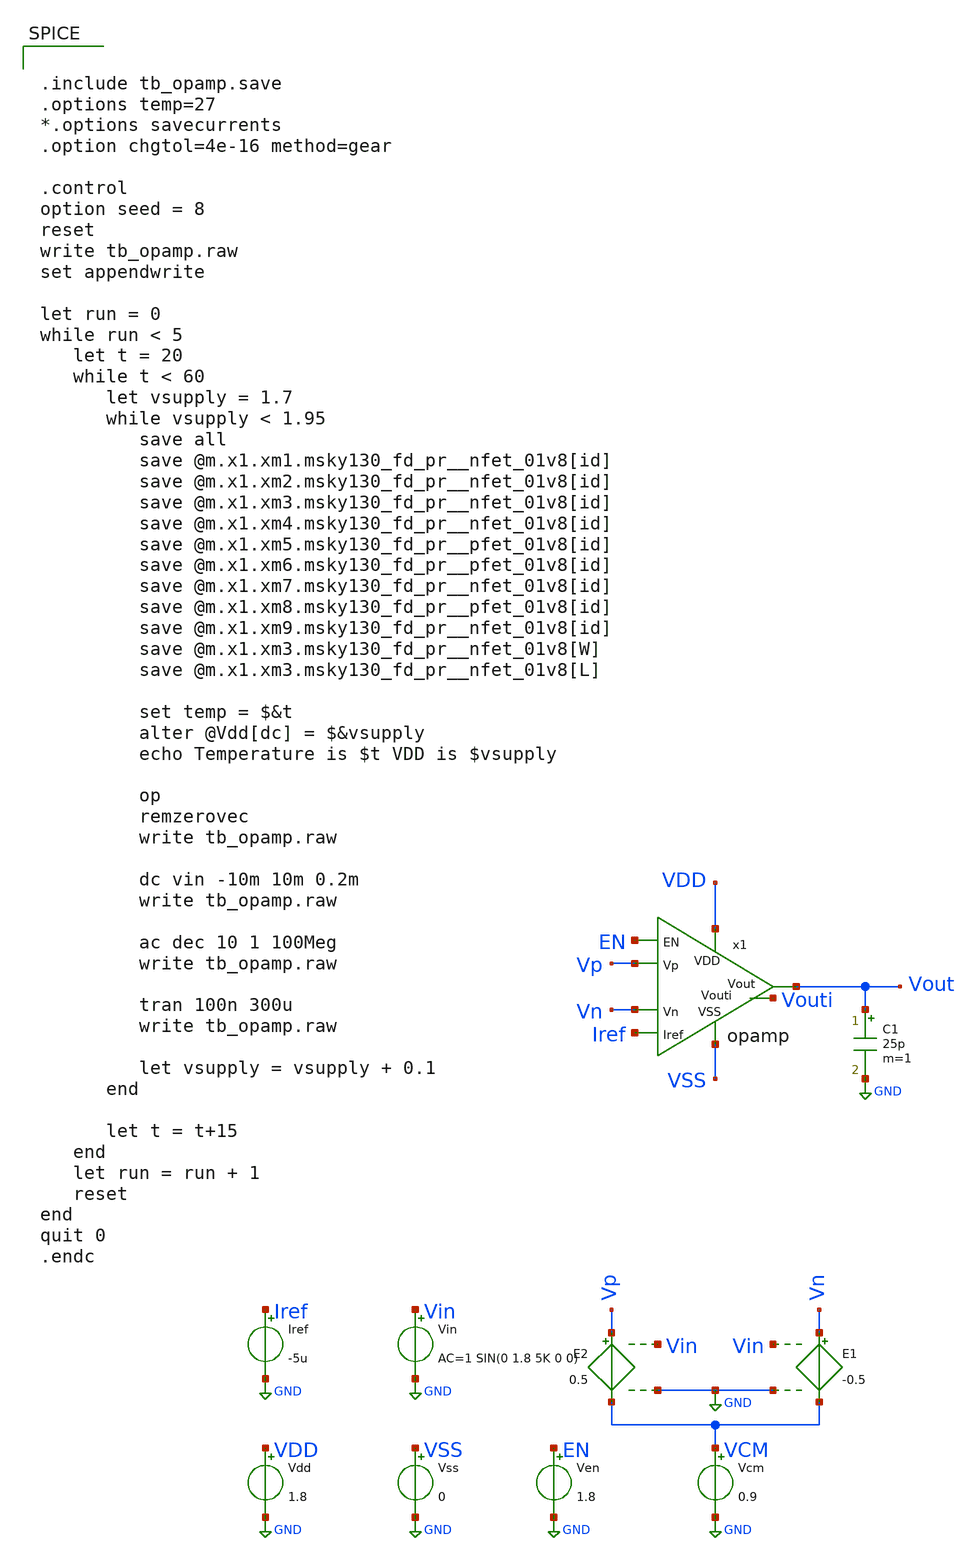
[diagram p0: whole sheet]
** sch_path: xschem/tb_opamp.sch
**.subckt tb_opamp
Vdd VDD GND 1.8
Vss VSS GND 0
E1 Vn VCM Vin GND -0.5
Vcm VCM GND 0.9
E2 Vp VCM Vin GND 0.5
Vin Vin GND AC=1 SIN(0 1.8 5K 0 0)
Iref Iref GND -5u
x1 Vout Vn Vp VSS Iref VDD Vouti EN opamp
Ven EN GND 1.8
C1 Vout GND 25p m=1
**** begin user architecture code


.include tb_opamp.save
.options temp=27
*.options savecurrents
.option chgtol=4e-16 method=gear

.control
option seed = 8
reset
write tb_opamp.raw
set appendwrite

let run = 0
while run < 5
   let t = 20
   while t < 60
      let vsupply = 1.7
      while vsupply < 1.95
         save all
         save @m.x1.xm1.msky130_fd_pr__nfet_01v8[id]
         save @m.x1.xm2.msky130_fd_pr__nfet_01v8[id]
         save @m.x1.xm3.msky130_fd_pr__nfet_01v8[id]
         save @m.x1.xm4.msky130_fd_pr__nfet_01v8[id]
         save @m.x1.xm5.msky130_fd_pr__pfet_01v8[id]
         save @m.x1.xm6.msky130_fd_pr__pfet_01v8[id]
         save @m.x1.xm7.msky130_fd_pr__nfet_01v8[id]
         save @m.x1.xm8.msky130_fd_pr__pfet_01v8[id]
         save @m.x1.xm9.msky130_fd_pr__nfet_01v8[id]
         save @m.x1.xm3.msky130_fd_pr__nfet_01v8[W]
         save @m.x1.xm3.msky130_fd_pr__nfet_01v8[L]

         set temp = $&t
         alter @Vdd[dc] = $&vsupply
         echo Temperature is $t VDD is $vsupply

         op
         remzerovec
         write tb_opamp.raw

         dc vin -10m 10m 0.2m
         write tb_opamp.raw

         ac dec 10 1 100Meg
         write tb_opamp.raw

         tran 100n 300u
         write tb_opamp.raw

         let vsupply = vsupply + 0.1
      end

      let t = t+15
   end
   let run = run + 1
   reset
end
quit 0
.endc



** opencircuitdesign pdks install
.param MT_SWITCH = 1.0
.lib $::SKYWATER_MODELS/sky130.lib.spice tt_mm

**** end user architecture code
**.ends

* expanding   symbol:  /foss/designs/ttsky_opamp/xschem/opamp.sym # of pins=8
** sym_path: xschem/opamp.sym
** sch_path: xschem/opamp.sch
.subckt opamp Vout Vn Vp VSS Iref VDD Vouti EN
*.ipin VSS
*.ipin Vp
*.opin Vout
*.ipin Vn
*.ipin VDD
*.ipin Iref
*.opin Vouti
*.ipin EN
XM1 VGref VGref VSS VSS sky130_fd_pr__nfet_01v8 L=0.5 W=4 nf=4 ad='int((4 + 1)/2) * 4 / 4 * 0.29' as='int((4 + 2)/2) * 4 / 4 * 0.29'
+ pd='2*int((4 + 1)/2) * (4 / 4 + 0.29)' ps='2*int((4 + 2)/2) * (4 / 4 + 0.29)' nrd='0.29 / 4 ' nrs='0.29 / 4 '
+ sa=0 sb=0 sd=0 mult=1 m=1
XM2 Vx VGref VSS VSS sky130_fd_pr__nfet_01v8 L=0.5 W=4 nf=4 ad='int((4 + 1)/2) * 4 / 4 * 0.29' as='int((4 + 2)/2) * 4 / 4 * 0.29'
+ pd='2*int((4 + 1)/2) * (4 / 4 + 0.29)' ps='2*int((4 + 2)/2) * (4 / 4 + 0.29)' nrd='0.29 / 4 ' nrs='0.29 / 4 '
+ sa=0 sb=0 sd=0 mult=1 m=1
XM3 Vouti Vp Vx VSS sky130_fd_pr__nfet_01v8 L=4 W=10 nf=4 ad='int((4 + 1)/2) * 10 / 4 * 0.29' as='int((4 + 2)/2) * 10 / 4 * 0.29'
+ pd='2*int((4 + 1)/2) * (10 / 4 + 0.29)' ps='2*int((4 + 2)/2) * (10 / 4 + 0.29)' nrd='0.29 / 10 ' nrs='0.29 / 10 '
+ sa=0 sb=0 sd=0 mult=1 m=1
XM4 Vg2 Vn Vx VSS sky130_fd_pr__nfet_01v8 L=4 W=10 nf=4 ad='int((4 + 1)/2) * 10 / 4 * 0.29' as='int((4 + 2)/2) * 10 / 4 * 0.29'
+ pd='2*int((4 + 1)/2) * (10 / 4 + 0.29)' ps='2*int((4 + 2)/2) * (10 / 4 + 0.29)' nrd='0.29 / 10 ' nrs='0.29 / 10 '
+ sa=0 sb=0 sd=0 mult=1 m=1
XM5 Vouti Vg2 VDD VDD sky130_fd_pr__pfet_01v8 L=4 W=12 nf=2 ad='int((2 + 1)/2) * 12 / 2 * 0.29' as='int((2 + 2)/2) * 12 / 2 * 0.29'
+ pd='2*int((2 + 1)/2) * (12 / 2 + 0.29)' ps='2*int((2 + 2)/2) * (12 / 2 + 0.29)' nrd='0.29 / 12 ' nrs='0.29 / 12 '
+ sa=0 sb=0 sd=0 mult=1 m=1
XM6 Vg2 Vg2 VDD VDD sky130_fd_pr__pfet_01v8 L=4 W=12 nf=2 ad='int((2 + 1)/2) * 12 / 2 * 0.29' as='int((2 + 2)/2) * 12 / 2 * 0.29'
+ pd='2*int((2 + 1)/2) * (12 / 2 + 0.29)' ps='2*int((2 + 2)/2) * (12 / 2 + 0.29)' nrd='0.29 / 12 ' nrs='0.29 / 12 '
+ sa=0 sb=0 sd=0 mult=1 m=1
XM7 Vout VGref VSS VSS sky130_fd_pr__nfet_01v8 L=0.5 W=48 nf=48 ad='int((48 + 1)/2) * 48 / 48 * 0.29'
+ as='int((48 + 2)/2) * 48 / 48 * 0.29' pd='2*int((48 + 1)/2) * (48 / 48 + 0.29)' ps='2*int((48 + 2)/2) * (48 / 48 + 0.29)'
+ nrd='0.29 / 48 ' nrs='0.29 / 48 ' sa=0 sb=0 sd=0 mult=1 m=1
XM8 Vout Vouti VDD VDD sky130_fd_pr__pfet_01v8 L=0.5 W=20 nf=4 ad='int((4 + 1)/2) * 20 / 4 * 0.29' as='int((4 + 2)/2) * 20 / 4 * 0.29'
+ pd='2*int((4 + 1)/2) * (20 / 4 + 0.29)' ps='2*int((4 + 2)/2) * (20 / 4 + 0.29)' nrd='0.29 / 20 ' nrs='0.29 / 20 '
+ sa=0 sb=0 sd=0 mult=1 m=1
XM9 Iref EN VGref VSS sky130_fd_pr__nfet_01v8 L=2 W=2 nf=1 ad='int((1 + 1)/2) * 2 / 1 * 0.29' as='int((1 + 2)/2) * 2 / 1 * 0.29'
+ pd='2*int((1 + 1)/2) * (2 / 1 + 0.29)' ps='2*int((1 + 2)/2) * (2 / 1 + 0.29)' nrd='0.29 / 2 ' nrs='0.29 / 2 '
+ sa=0 sb=0 sd=0 mult=1 m=1
XC1 Vout net1 sky130_fd_pr__cap_mim_m3_1 W=30 L=30 MF=1 m=1
XR3 net1 Vouti VSS sky130_fd_pr__res_xhigh_po_0p35 L=5 mult=1 m=1
XM11 Vx VSS VSS VSS sky130_fd_pr__nfet_01v8 L=4 W=10 nf=2 ad='int((2 + 1)/2) * 10 / 2 * 0.29' as='int((2 + 2)/2) * 10 / 2 * 0.29'
+ pd='2*int((2 + 1)/2) * (10 / 2 + 0.29)' ps='2*int((2 + 2)/2) * (10 / 2 + 0.29)' nrd='0.29 / 10 ' nrs='0.29 / 10 '
+ sa=0 sb=0 sd=0 mult=1 m=1
XM12 VSS VSS VSS VSS sky130_fd_pr__nfet_01v8 L=0.5 W=2 nf=2 ad='int((2 + 1)/2) * 2 / 2 * 0.29' as='int((2 + 2)/2) * 2 / 2 * 0.29'
+ pd='2*int((2 + 1)/2) * (2 / 2 + 0.29)' ps='2*int((2 + 2)/2) * (2 / 2 + 0.29)' nrd='0.29 / 2 ' nrs='0.29 / 2 '
+ sa=0 sb=0 sd=0 mult=1 m=1
XM10 Vouti VDD VDD VDD sky130_fd_pr__pfet_01v8 L=4 W=12 nf=2 ad='int((2 + 1)/2) * 12 / 2 * 0.29' as='int((2 + 2)/2) * 12 / 2 * 0.29'
+ pd='2*int((2 + 1)/2) * (12 / 2 + 0.29)' ps='2*int((2 + 2)/2) * (12 / 2 + 0.29)' nrd='0.29 / 12 ' nrs='0.29 / 12 '
+ sa=0 sb=0 sd=0 mult=1 m=1
XM13 VDD VDD VDD VDD sky130_fd_pr__pfet_01v8 L=0.5 W=10 nf=2 ad='int((2 + 1)/2) * 10 / 2 * 0.29' as='int((2 + 2)/2) * 10 / 2 * 0.29'
+ pd='2*int((2 + 1)/2) * (10 / 2 + 0.29)' ps='2*int((2 + 2)/2) * (10 / 2 + 0.29)' nrd='0.29 / 10 ' nrs='0.29 / 10 '
+ sa=0 sb=0 sd=0 mult=1 m=1
.ends

.GLOBAL GND
.GLOBAL VDD
.end
